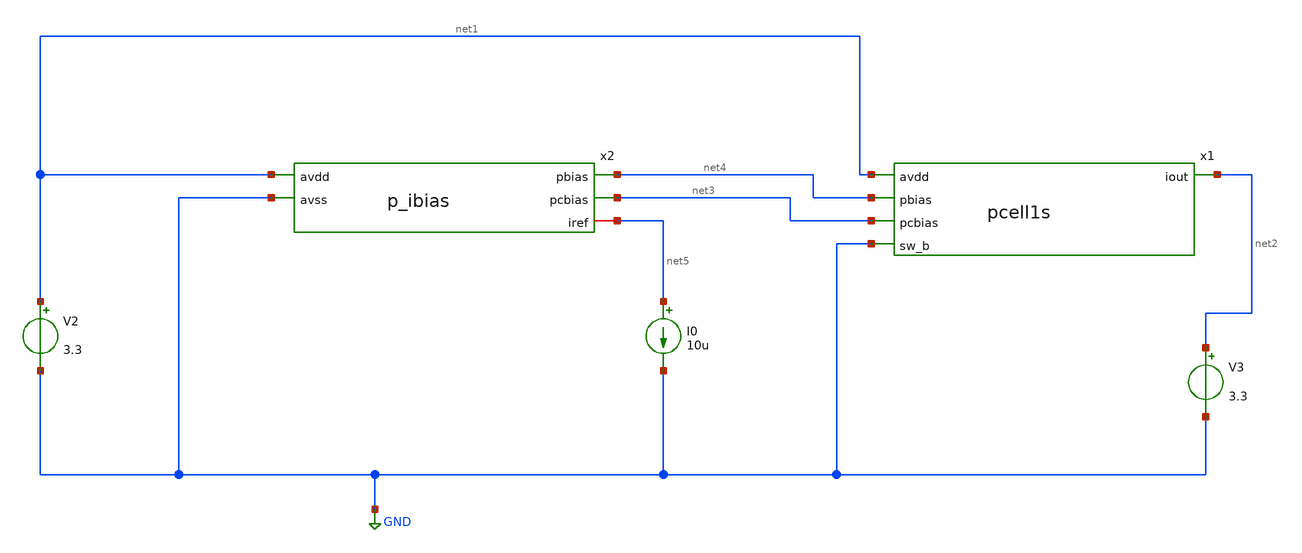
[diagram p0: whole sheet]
** sch_path: xschem/currentmirrorPtests_tb.sch
**.subckt currentmirrorPtests_tb
V2 net1 GND 3.3
V3 net2 GND 3.3
x1 net1 net4 net3 GND net2 pcell1s
x2 net1 net4 net3 net5 GND p_ibias
I0 net5 GND 10u
**** begin user architecture code
 .lib $::SKYWATER_MODELS/sky130.lib.spice tt

.param mc_mm_switch=0
.param mc_pr_switch=1



.option wnflag=0
.option savecurrents
.control
save all
dc v3 0 3.3 0.01
plot i(V3)
write currentmirrortb.raw
op
.endc


 .lib $::SKYWATER_MODELS/sky130.lib.spice tt

.param mc_mm_switch=0
.param mc_pr_switch=1



.option wnflag=0
.option savecurrents
.control
save all
dc v3 0 3.3 0.01
plot i(V3)
write currentmirrortb.raw
op
.endc


**** end user architecture code
**.ends

* expanding   symbol:  pcell1s.sym # of pins=5
** sym_path: xschem/pcell1s.sym
** sch_path: xschem/pcell1s.sch
.subckt pcell1s avdd pbias pcbias sw_b iout
*.ipin pbias
*.ipin pcbias
*.ipin sw_b
*.ipin avdd
*.opin iout
XM1 net1 pbias avdd avdd sky130_fd_pr__pfet_g5v0d10v5 L=0.5 W=6 nf=1 ad='int((nf+1)/2) * W/nf * 0.29'
+ as='int((nf+2)/2) * W/nf * 0.29' pd='2*int((nf+1)/2) * (W/nf + 0.29)' ps='2*int((nf+2)/2) * (W/nf + 0.29)'
+ nrd='0.29 / W' nrs='0.29 / W' sa=0 sb=0 sd=0 mult=1 m=1
XM2 net2 pcbias net1 avdd sky130_fd_pr__pfet_g5v0d10v5 L=0.5 W=12 nf=1 ad='int((nf+1)/2) * W/nf * 0.29'
+ as='int((nf+2)/2) * W/nf * 0.29' pd='2*int((nf+1)/2) * (W/nf + 0.29)' ps='2*int((nf+2)/2) * (W/nf + 0.29)'
+ nrd='0.29 / W' nrs='0.29 / W' sa=0 sb=0 sd=0 mult=1 m=1
XM3 iout sw_b net2 avdd sky130_fd_pr__pfet_g5v0d10v5 L=0.5 W=4 nf=1 ad='int((nf+1)/2) * W/nf * 0.29'
+ as='int((nf+2)/2) * W/nf * 0.29' pd='2*int((nf+1)/2) * (W/nf + 0.29)' ps='2*int((nf+2)/2) * (W/nf + 0.29)'
+ nrd='0.29 / W' nrs='0.29 / W' sa=0 sb=0 sd=0 mult=1 m=1
.ends


* expanding   symbol:  p_ibias.sym # of pins=5
** sym_path: xschem/p_ibias.sym
** sch_path: xschem/p_ibias.sch
.subckt p_ibias avdd pbias pcbias iref avss
*.ipin avdd
*.iopin iref
*.ipin avss
*.opin pbias
*.opin pcbias
XM3 pcbias pcbias avdd avdd sky130_fd_pr__pfet_g5v0d10v5 L=12 W=8 nf=1 ad='int((nf+1)/2) * W/nf * 0.29'
+ as='int((nf+2)/2) * W/nf * 0.29' pd='2*int((nf+1)/2) * (W/nf + 0.29)' ps='2*int((nf+2)/2) * (W/nf + 0.29)'
+ nrd='0.29 / W' nrs='0.29 / W' sa=0 sb=0 sd=0 mult=1 m=1
XM4 net1 pbias avdd avdd sky130_fd_pr__pfet_g5v0d10v5 L=0.5 W=6 nf=1 ad='int((nf+1)/2) * W/nf * 0.29'
+ as='int((nf+2)/2) * W/nf * 0.29' pd='2*int((nf+1)/2) * (W/nf + 0.29)' ps='2*int((nf+2)/2) * (W/nf + 0.29)'
+ nrd='0.29 / W' nrs='0.29 / W' sa=0 sb=0 sd=0 mult=1 m=1
XM5 pbias pcbias net1 avdd sky130_fd_pr__pfet_g5v0d10v5 L=0.5 W=12 nf=1 ad='int((nf+1)/2) * W/nf * 0.29'
+ as='int((nf+2)/2) * W/nf * 0.29' pd='2*int((nf+1)/2) * (W/nf + 0.29)' ps='2*int((nf+2)/2) * (W/nf + 0.29)'
+ nrd='0.29 / W' nrs='0.29 / W' sa=0 sb=0 sd=0 mult=1 m=1
XM6 iref iref avdd avdd sky130_fd_pr__pfet_g5v0d10v5 L=0.5 W=8 nf=1 ad='int((nf+1)/2) * W/nf * 0.29'
+ as='int((nf+2)/2) * W/nf * 0.29' pd='2*int((nf+1)/2) * (W/nf + 0.29)' ps='2*int((nf+2)/2) * (W/nf + 0.29)'
+ nrd='0.29 / W' nrs='0.29 / W' sa=0 sb=0 sd=0 mult=1 m=1
XM1 pbias net2 avss avss sky130_fd_pr__nfet_g5v0d10v5 L=0.5 W=4.5 nf=1 ad='int((nf+1)/2) * W/nf * 0.29'
+ as='int((nf+2)/2) * W/nf * 0.29' pd='2*int((nf+1)/2) * (W/nf + 0.29)' ps='2*int((nf+2)/2) * (W/nf + 0.29)'
+ nrd='0.29 / W' nrs='0.29 / W' sa=0 sb=0 sd=0 mult=1 m=1
XM2 net3 iref avdd avdd sky130_fd_pr__pfet_g5v0d10v5 L=0.5 W=8 nf=1 ad='int((nf+1)/2) * W/nf * 0.29'
+ as='int((nf+2)/2) * W/nf * 0.29' pd='2*int((nf+1)/2) * (W/nf + 0.29)' ps='2*int((nf+2)/2) * (W/nf + 0.29)'
+ nrd='0.29 / W' nrs='0.29 / W' sa=0 sb=0 sd=0 mult=1 m=1
XM7 net2 net2 avss avss sky130_fd_pr__nfet_g5v0d10v5 L=0.5 W=10 nf=1 ad='int((nf+1)/2) * W/nf * 0.29'
+ as='int((nf+2)/2) * W/nf * 0.29' pd='2*int((nf+1)/2) * (W/nf + 0.29)' ps='2*int((nf+2)/2) * (W/nf + 0.29)'
+ nrd='0.29 / W' nrs='0.29 / W' sa=0 sb=0 sd=0 mult=1 m=1
XM8 pcbias net2 avss avss sky130_fd_pr__nfet_g5v0d10v5 L=0.5 W=4.5 nf=1 ad='int((nf+1)/2) * W/nf * 0.29'
+ as='int((nf+2)/2) * W/nf * 0.29' pd='2*int((nf+1)/2) * (W/nf + 0.29)' ps='2*int((nf+2)/2) * (W/nf + 0.29)'
+ nrd='0.29 / W' nrs='0.29 / W' sa=0 sb=0 sd=0 mult=1 m=1
XM9 net2 net2 net3 avdd sky130_fd_pr__pfet_g5v0d10v5 L=0.5 W=8 nf=1 ad='int((nf+1)/2) * W/nf * 0.29'
+ as='int((nf+2)/2) * W/nf * 0.29' pd='2*int((nf+1)/2) * (W/nf + 0.29)' ps='2*int((nf+2)/2) * (W/nf + 0.29)'
+ nrd='0.29 / W' nrs='0.29 / W' sa=0 sb=0 sd=0 mult=1 m=1
.ends

.GLOBAL GND
.end
